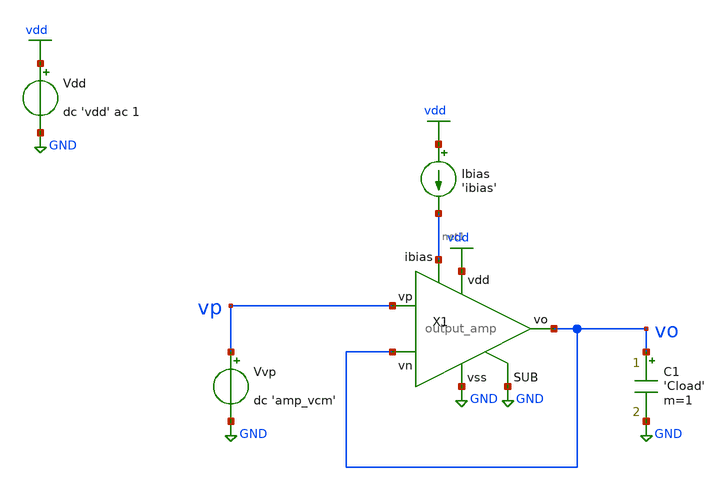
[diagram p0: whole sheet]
** sch_path: tb/output_amp/tb_amp_noise.sch
**.subckt tb_amp_noise
X1 vdd vo vp vo net1 GND GND output_amp
Vdd vdd GND dc 'vdd' ac 1
Vvp vp GND dc 'amp_vcm'
Ibias vdd net1 'ibias'
C1 vo GND 'Cload' m=1
**** begin user architecture code


.lib 'models_dir'/cornerMOShv.lib 'mos_corner'
.lib 'models_dir'/cornerCAP.lib cap_typ
.preprocess replaceground true
.option temp='temperature'
.op
.noise v(vo) Vdd dec 20 'frequency_start' 'frequency_stop'
.print noise file='simpath'/'filename'_'N'.data ONOISE


**** end user architecture code
**.ends
.GLOBAL GND
.GLOBAL vdd
.end
